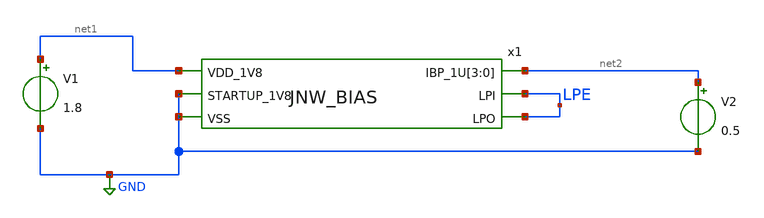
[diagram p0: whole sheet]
** sch_path: design/JNW_BIAS_SKY130A/TB_JNW_BIAS.sch
**.subckt TB_JNW_BIAS
x1 net1 LPE net2 net2 net2 net2 LPE GND GND JNW_BIAS
V1 net1 GND 1.8
V2 net2 GND 0.5
**** begin user architecture code



* ngspice commands
.include corner.spi



**** end user architecture code
**.ends
.GLOBAL GND
.end
